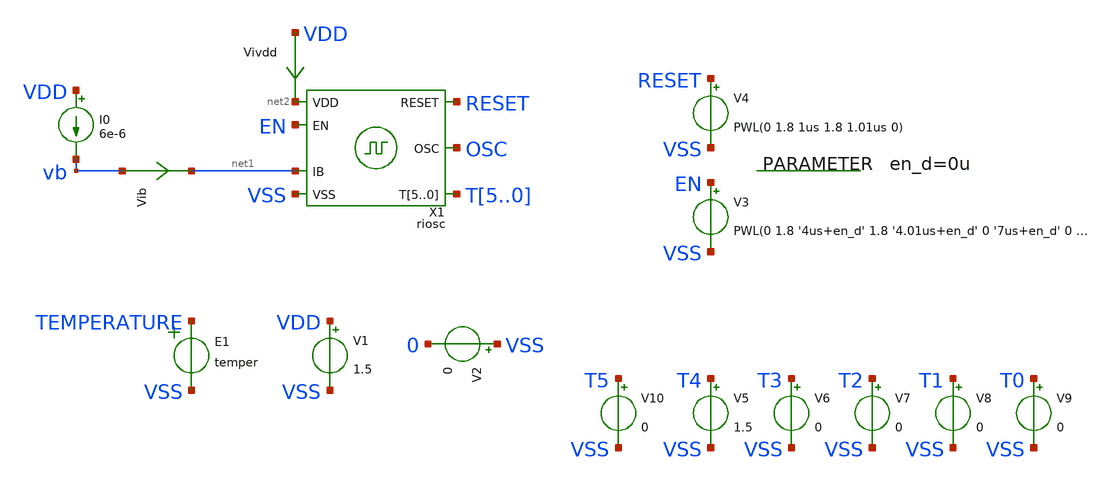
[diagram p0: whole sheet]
** sch_path: ip/riosc/xschem/riosc_tb.sch
* IHP-GmbH/IHP-Open-PDK/ihp-sg13g2/libs.tech/xschem/sg13g2_stdcells/sg13g2_inv_4.sch:
* Copyright 2023 IHP PDK Authors
* Licensed under the Apache License, Version 2.0 (the "License");
**.subckt riosc_tb
V1 VDD VSS 1.5
V2 VSS 0 0
E1 TEMPERATURE VSS VOL=' temper '
I0 VDD vb 6e-6
Vib vb net1 0
.save i(vib)
V3 EN VSS PWL(0 1.8 '4us+en_d' 1.8 '4.01us+en_d' 0 '7us+en_d' 0 '7.01us+en_d' 1.8)
V4 RESET VSS PWL(0 1.8 1us 1.8 1.01us 0)
.param en_d=0u
Vivdd VDD net2 0
.save i(vivdd)
V5 T4 VSS 1.5
V6 T3 VSS 0
V7 T2 VSS 0
V8 T1 VSS 0
V9 T0 VSS 0
V10 T5 VSS 0
X1 net2 VSS OSC EN net1 RESET T5 T4 T3 T2 T1 T0 riosc
**** begin user architecture code

.csparam TB_ID=${::TB_ID}
.csparam MC_RUNS=${::MC_RUNS}
.csparam EXIT_NGSPICE=${::EXIT_NGSPICE}
.lib ${::IHP_MODELS}/sg13g2.lib ${::CORNER}


* this experimental option enables mos model bin
* selection based on W/NF instead of W
.option wnflag=0
.option warn=0

.control
* option savecurrents
*save all


* dummy block for goto
if (1)
if TB_ID = 0
	goto TRAN
end
if TB_ID = 1
	goto TRAN
end
if TB_ID = 2
	goto TRAN_PEX
end

****************************************
label TRAN
*save all
label TRAN_PEX
*save all
****************************************
if MC_RUNS = 0
	let veclen=9
	let en_dt = vector(veclen)
	let vs = vector(veclen)
	let temp = vector(veclen)
	let first_high = vector(veclen)
	let first_period = vector(veclen)
	let first_dutycycle_percent = vector(veclen)
	let last_high = vector(veclen)
	let run = 0
	foreach te -40 20 125
	*foreach te 20
	*foreach en_delay 0 0.1us 0.2us
	*foreach en_delay 0
		foreach vsup 1.5 1.8 1.9
		*foreach vsup 1.5
			*alterparam en_d = $en_delay
			*reset
			alter v1=$vsup
			option temp=$te
			*save OSC, EN, VDD, x1.ENA_D1, x1.RESETB, TEMPERATURE
			save OSC, vb, EN, VDD, TEMPERATURE, x1.ENA_D1, x1.ENA1, x1.ENA2

			tran 200p 10u
			meas tran m_high_v find v(VDD) at=1u
			meas tran m_temp find v(TEMPERATURE) at=1u
			let vddz = {m_high_v/2}
			meas tran m_first_high trig v(OSC) val=vddz td=5u rise=1 targ v(OSC) val=vddz td=5u fall=1
			meas tran m_first_per trig v(OSC) val=vddz td=5u rise=1 targ v(OSC) val=vddz td=5u rise=2
			meas tran m_en_t when v(x1.ENA_D1)=vddz fall=1
			meas tran m_last_rising_t when v(OSC)=vddz td=m_en_t rise=1
			meas tran m_last_falling_t when v(OSC)=vddz td=m_last_rising_t fall=1
			*meas tran m_last_high trig v(OSC) val=vddz td=m_en_t rise=1 targ v(OSC) val=vddz td=m_en_t
+ fall=1
			let m_last_high = m_last_falling_t-m_last_rising_t

			*plot Temperature
			*plot Vib#branch
			*plot Vivdd#branch
			*plot vb
			plot OSC
			*plot OSC EN x1.ENA_D1 x1.RESETB
			*plot EN
			*plot x1.ENA_D1
                        *plot x1.ENA1, x1.ENA2
			*plot x1.RESETB
			let en_dt[run] = 0
			let vs[run] = m_high_v
			let temp[run] = m_temp
			let first_high[run] = m_first_high
			let first_period[run] = m_first_per
			let first_dutycycle_percent[run] = {100/m_first_per*m_first_high}
			let last_high[run] = $&m_last_high
			let run = run + 1
			write tran.raw all
			set appendwrite
		end
	end
	set nobreak
	set width=300
	print en_dt, temp, vs, first_high, first_period, first_dutycycle_percent, last_high > tran.csv
else
	define aunif(nom, avar) (nom+avar*sunif(0))
	define agauss(nom, avar, sig) (nom + avar / sig * sgauss (0))
	let en_dt = vector(MC_RUNS)
	let vs = vector(MC_RUNS)
	let temp = vector(MC_RUNS)
	let first_high = vector(MC_RUNS)
	let first_period = vector(MC_RUNS)
	let first_dutycycle_percent = vector(MC_RUNS)
	let last_high = vector(MC_RUNS)
	let run=0
	dowhile run < MC_RUNS
		echo MC-RUN: $&run
		let ti = aunif(0, 200e-9)
		alterparam en_d = $&ti
		reset
		let vsup = aunif(1.7, 0.2)
		alter v1=$&vsup
		let te = aunif(50, 90)
		option temp=$&te
		save OSC, EN, VDD, TEMPERATURE, x1.ENA_D1

		tran 200p 10u
		meas tran m_high_v find v(VDD) at=1u
		let vddz = {m_high_v/2}
		meas tran m_first_high trig v(OSC) val=vddz td=5u rise=1 targ v(OSC) val=vddz td=5u fall=1
		meas tran m_first_per trig v(OSC) val=vddz td=5u rise=1 targ v(OSC) val=vddz td=5u rise=2
		meas tran m_en_t when v(x1.ENA_D1)=vddz fall=1
		meas tran m_last_rising_t when v(OSC)=vddz td=m_en_t rise=1
		meas tran m_last_falling_t when v(OSC)=vddz td=m_last_rising_t fall=1
		*meas tran m_last_high trig v(OSC) val=vddz td=m_en_t rise=1 targ v(OSC) val=vddz td=m_en_t fall=1
		let m_last_high = m_last_falling_t-m_last_rising_t

		let en_dt[run] = $&ti
		let vs[run] = $&vsup
		let temp[run] = $&te
		let first_high[run] = m_first_high
		let first_period[run] = m_first_per
		let first_dutycycle_percent[run] = {100/m_first_per*m_first_high}
		let last_high[run] = $&m_last_high
		let run = run + 1
	end
	set nobreak
	set width=300
	print en_dt, temp, vs, first_high, first_period, first_dutycycle_percent, last_high > tran.csv
end
goto done

****************************************
label done
****************************************
if EXIT_NGSPICE > 0.0
	exit
end
end
.endc



.include ${::IHP_STDCELLS}/sg13g2_stdcell.spice

**** end user architecture code
**.ends

* expanding   symbol:  riosc.sym # of pins=7
** sym_path: ip/riosc/xschem/riosc.sym
** sch_path: ip/riosc/xschem/riosc.sch
.subckt riosc VDD VSS OSC EN IB RESET T5 T4 T3 T2 T1 T0
*.iopin VSS
*.iopin VDD
*.ipin IB
*.opin OSC
*.ipin EN
*.ipin RESET
*.ipin T5,T4,T3,T2,T1,T0
x8 RESETB RESET VDD VSS sg13g2_inv_4
x5 ENA1 ENA2 VDD VSS sg13g2_inv_4
x6 ENA2 EN net19 VDD VSS sg13g2_or2_2
x1 net18 net26 OSC_N EN RESETB VDD VSS sg13g2_dfrbp_2
x2 ENA_D1 net27 OSC_N net18 RESETB VDD VSS sg13g2_dfrbp_2
x3 net19 net28 OSC_N ENA_D1 RESETB VDD VSS sg13g2_dfrbp_2
x4 OSC net10 VDD VSS sg13g2_inv_4
x7 OSC_N OSC VDD VSS sg13g2_inv_4
XM1 net5 ENA1 VSS VSS sg13_lv_nmos w=2u l=0.5u ng=1 m=1 mm_ok=1
XM2 net16 ENA2 net5 VSS sg13_lv_nmos w=2u l=0.5u ng=1 m=1 mm_ok=1
XM3 net2 net1 VDD VDD sg13_lv_pmos w=2u l=0.5u ng=1 m=1 mm_ok=1
XM4 net6 net1 VDD VDD sg13_lv_pmos w=2u l=0.5u ng=1 m=1 mm_ok=1
XM5 net9 net1 VDD VDD sg13_lv_pmos w=2u l=0.5u ng=1 m=1 mm_ok=1
XM6 net12 net1 VDD VDD sg13_lv_pmos w=2u l=0.5u ng=1 m=1 mm_ok=1
XM7 net15 net1 VDD VDD sg13_lv_pmos w=2u l=0.5u ng=1 m=1 mm_ok=1
XM8 net1 net1 VDD VDD sg13_lv_pmos w=2u l=0.5u ng=1 m=1 mm_ok=1
XM9 net3 net5 net2 VDD sg13_lv_pmos w=2u l=0.5u ng=1 m=1 mm_ok=1
XM10 net7 net3 net6 VDD sg13_lv_pmos w=2u l=0.5u ng=1 m=1 mm_ok=1
XM11 net10 net7 net9 VDD sg13_lv_pmos w=2u l=0.5u ng=1 m=1 mm_ok=1
XM12 net13 net10 net12 VDD sg13_lv_pmos w=2u l=0.5u ng=1 m=1 mm_ok=1
XM13 net16 net13 net15 VDD sg13_lv_pmos w=2u l=0.5u ng=1 m=1 mm_ok=1
XM14 net3 net5 net4 VSS sg13_lv_nmos w=2u l=0.5u ng=1 m=1 mm_ok=1
XM15 net7 net3 net8 VSS sg13_lv_nmos w=2u l=0.5u ng=1 m=1 mm_ok=1
XM16 net10 net7 net11 VSS sg13_lv_nmos w=2u l=0.5u ng=1 m=1 mm_ok=1
XM17 net13 net10 net14 VSS sg13_lv_nmos w=2u l=0.5u ng=1 m=1 mm_ok=1
XM18 net16 net13 net17 VSS sg13_lv_nmos w=2u l=0.5u ng=1 m=1 mm_ok=1
XM19 net1 IB VSS VSS sg13_lv_nmos w=2u l=0.5u ng=1 m=1 mm_ok=1
XM20 net4 IB VSS VSS sg13_lv_nmos w=2u l=0.5u ng=1 m=1 mm_ok=1
XM21 net8 IB VSS VSS sg13_lv_nmos w=2u l=0.5u ng=1 m=1 mm_ok=1
XM22 net11 IB VSS VSS sg13_lv_nmos w=2u l=0.5u ng=1 m=1 mm_ok=1
XM23 net14 IB VSS VSS sg13_lv_nmos w=2u l=0.5u ng=1 m=1 mm_ok=1
XM24 net17 IB VSS VSS sg13_lv_nmos w=2u l=0.5u ng=1 m=1 mm_ok=1
XM29 IB net20 VSS VSS sg13_lv_nmos w=0.25u l=0.5u ng=1 m=1 mm_ok=1
XM31 IB IB VSS VSS sg13_lv_nmos w=1u l=0.5u ng=1 m=1 mm_ok=1
x9 VDD IB T0 net20 VSS trimsw
XM25 IB net21 VSS VSS sg13_lv_nmos w=0.5u l=0.5u ng=1 m=1 mm_ok=1
x10 VDD IB T1 net21 VSS trimsw
XM26 IB net22 VSS VSS sg13_lv_nmos w=1u l=0.5u ng=1 m=1 mm_ok=1
x11 VDD IB T2 net22 VSS trimsw
XM27 IB net23 VSS VSS sg13_lv_nmos w=2u l=0.5u ng=1 m=1 mm_ok=1
x12 VDD IB T3 net23 VSS trimsw
XM28 IB net24 VSS VSS sg13_lv_nmos w=4u l=0.5u ng=1 m=1 mm_ok=1
x13 VDD IB T4 net24 VSS trimsw
XM30 IB net25 VSS VSS sg13_lv_nmos w=8u l=0.5u ng=1 m=1 mm_ok=1
x14 VDD IB T5 net25 VSS trimsw
.ends


* expanding   symbol:  sg13g2_stdcells/sg13g2_inv_4.sym # of pins=2
** sym_path: sg13g2_stdcells/sg13g2_inv_4.sym
** sch_path: sg13g2_stdcells/sg13g2_inv_4.sch
.subckt sg13g2_inv_4 Y A VDD VSS
*.ipin A
*.opin Y
*.iopin VDD
*.iopin VSS
XM1 Y A VSS VSS sg13_lv_nmos w=2.96u l=130.00n ng=4 m=1 mm_ok=1
XM2 Y A VDD VDD sg13_lv_pmos w=4.48u l=130.00n ng=4 m=1 mm_ok=1
.ends


* expanding   symbol:  sg13g2_stdcells/sg13g2_or2_2.sym # of pins=3
** sym_path: sg13g2_stdcells/sg13g2_or2_2.sym
** sch_path: sg13g2_stdcells/sg13g2_or2_2.sch
.subckt sg13g2_or2_2 X A B VDD VSS
*.opin X
*.ipin B
*.ipin A
*.iopin VDD
*.iopin VSS
XM1 net1 B VSS VSS sg13_lv_nmos w=550.00n l=130.00n ng=1 m=1 mm_ok=1
XM2 net1 A VSS VSS sg13_lv_nmos w=550.00n l=130.00n ng=1 m=1 mm_ok=1
XM3 X net1 VSS VSS sg13_lv_nmos w=1.48u l=130.00n ng=2 m=1 mm_ok=1
XM4 net2 A VDD VDD sg13_lv_pmos w=840.00n l=130.00n ng=1 m=1 mm_ok=1
XM5 net1 B net2 VDD sg13_lv_pmos w=840.00n l=130.00n ng=1 m=1 mm_ok=1
XM6 X net1 VDD VDD sg13_lv_pmos w=2.24u l=130.00n ng=2 m=1 mm_ok=1
.ends


* expanding   symbol:  sg13g2_stdcells/sg13g2_dfrbp_2.sym # of pins=5
** sym_path: sg13g2_stdcells/sg13g2_dfrbp_2.sym
** sch_path: sg13g2_stdcells/sg13g2_dfrbp_2.sch
.subckt sg13g2_dfrbp_2 Q Q_N CLK D RESET_B VDD VSS
*.ipin D
*.ipin RESET_B
*.ipin CLK
*.opin Q
*.opin Q_N
*.iopin VDD
*.iopin VSS
XM1 Db D net12 VSS sg13_lv_nmos w=420.00n l=130.00n ng=1 m=1 mm_ok=1
XM2 net12 RESET_B VSS VSS sg13_lv_nmos w=420.00n l=130.00n ng=1 m=1 mm_ok=1
XM3 net2 clkneg net11 VSS sg13_lv_nmos w=420.00n l=130.00n ng=1 m=1 mm_ok=1
XM4 net11 net3 VSS VSS sg13_lv_nmos w=420.00n l=130.00n ng=1 m=1 mm_ok=1
XM5 net3 net2 net7 VSS sg13_lv_nmos w=420.00n l=130.00n ng=1 m=1 mm_ok=1
XM6 net7 RESET_B VSS VSS sg13_lv_nmos w=420.00n l=130.00n ng=1 m=1 mm_ok=1
XM7 Q_N net2 VSS VSS sg13_lv_nmos w=1.48u l=130.00n ng=2 m=1 mm_ok=1
XM8 net1 net2 VSS VSS sg13_lv_nmos w=640.00n l=130.00n ng=1 m=1 mm_ok=1
XM9 Q net1 VSS VSS sg13_lv_nmos w=1.48u l=130.00n ng=2 m=1 mm_ok=1
XM10 clkneg CLK VSS VSS sg13_lv_nmos w=740.00n l=130.00n ng=1 m=1 mm_ok=1
XM11 clkpos clkneg VSS VSS sg13_lv_nmos w=740.00n l=130.00n ng=1 m=1 mm_ok=1
XM12 Db clkneg net4 VSS sg13_lv_nmos w=420.00n l=130.00n ng=1 m=1 mm_ok=1
XM13 net4 clkpos net10 VSS sg13_lv_nmos w=420.00n l=130.00n ng=1 m=1 mm_ok=1
XM14 net10 net5 net6 VSS sg13_lv_nmos w=420.00n l=130.00n ng=1 m=1 mm_ok=1
XM15 net6 RESET_B VSS VSS sg13_lv_nmos w=420.00n l=130.00n ng=1 m=1 mm_ok=1
XM16 net5 net4 VSS VSS sg13_lv_nmos w=740.00n l=130.00n ng=1 m=1 mm_ok=1
XM17 net5 clkpos net2 VSS sg13_lv_nmos w=740.00n l=130.00n ng=1 m=1 mm_ok=1
XM18 Db RESET_B VDD VDD sg13_lv_pmos w=420.00n l=130.00n ng=1 m=1 mm_ok=1
XM19 Db D VDD VDD sg13_lv_pmos w=420.00n l=130.00n ng=1 m=1 mm_ok=1
XM20 net9 net3 VDD VDD sg13_lv_pmos w=420.00n l=130.00n ng=1 m=1 mm_ok=1
XM21 net2 clkpos net9 VDD sg13_lv_pmos w=420.00n l=130.00n ng=1 m=1 mm_ok=1
XM22 net3 net2 VDD VDD sg13_lv_pmos w=420.00n l=130.00n ng=1 m=1 mm_ok=1
XM23 net3 RESET_B VDD VDD sg13_lv_pmos w=420.00n l=130.00n ng=1 m=1 mm_ok=1
XM24 Q_N net2 VDD VDD sg13_lv_pmos w=2.24u l=130.00n ng=2 m=1 mm_ok=1
XM25 net1 net2 VDD VDD sg13_lv_pmos w=1.000u l=130.00n ng=1 m=1 mm_ok=1
XM26 Q net1 VDD VDD sg13_lv_pmos w=2.24u l=130.00n ng=2 m=1 mm_ok=1
XM27 clkneg CLK VDD VDD sg13_lv_pmos w=1.12u l=130.00n ng=1 m=1 mm_ok=1
XM28 clkpos clkneg VDD VDD sg13_lv_pmos w=1.12u l=130.00n ng=1 m=1 mm_ok=1
XM29 Db clkpos net4 VDD sg13_lv_pmos w=420.00n l=130.00n ng=1 m=1 mm_ok=1
XM30 net8 net5 VDD VDD sg13_lv_pmos w=420.00n l=130.00n ng=1 m=1 mm_ok=1
XM31 net4 clkneg net8 VDD sg13_lv_pmos w=420.00n l=130.00n ng=1 m=1 mm_ok=1
XM32 net4 RESET_B VDD VDD sg13_lv_pmos w=420.00n l=130.00n ng=1 m=1 mm_ok=1
XM33 net5 net4 VDD VDD sg13_lv_pmos w=1.000u l=130.00n ng=1 m=1 mm_ok=1
XM34 net5 clkneg net2 VDD sg13_lv_pmos w=1.000u l=130.00n ng=1 m=1 mm_ok=1
.ends


* expanding   symbol:  trimsw.sym # of pins=5
** sym_path: ip/riosc/xschem/trimsw.sym
** sch_path: ip/riosc/xschem/trimsw.sch
.subckt trimsw VDD T EN G VSS
*.iopin G
*.iopin VSS
*.iopin T
*.ipin EN
*.iopin VDD
XM1 G net1 VSS VSS sg13_lv_nmos w=0.5u l=0.25u ng=1 m=1 mm_ok=1
XM2 T net2 G VSS sg13_lv_nmos w=0.5u l=0.25u ng=1 m=1 mm_ok=1
x1 net1 EN VDD VSS sg13g2_not_1
x2 net2 net1 VDD VSS sg13g2_not_1
.ends

.end
